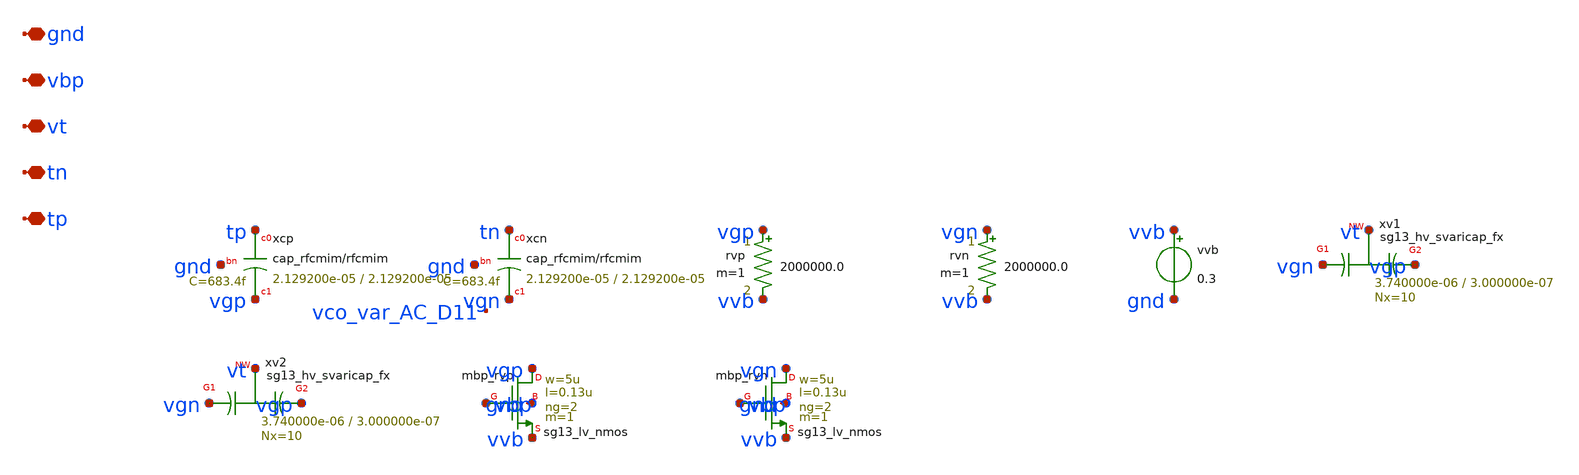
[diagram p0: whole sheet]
** sch_path: analog/vco/sch/vco_var.sch
**.subckt vco_var tp tn vt vbp gnd
*.iopin tp
*.iopin tn
*.iopin vt
*.iopin vbp
*.iopin gnd
Xxcp tp vgp gnd cap_rfcmim w=2.129200e-05 l=2.129200e-05 wfeed=5.0e-6 m=1 mm_ok=1
Xxcn tn vgn gnd cap_rfcmim w=2.129200e-05 l=2.129200e-05 wfeed=5.0e-6 m=1 mm_ok=1
rvp vgp vvb 2000000.0 m=1
rvn vgn vvb 2000000.0 m=1
vvb vvb gnd 0.3
Xxv1 vgn vt vgp sub! sg13_hv_svaricap_fx w=3.740000e-06 l=3.000000e-07 Nx=10 mm_ok=1
Xxv2 vgn vt vgp sub! sg13_hv_svaricap_fx w=3.740000e-06 l=3.000000e-07 Nx=10 mm_ok=1
Xmbp_rvp vgp vbp vvb gnd sg13_lv_nmos w=5u l=0.13u ng=2 m=1 mm_ok=1
Xmbp_rvn vgn vbp vvb gnd sg13_lv_nmos w=5u l=0.13u ng=2 m=1 mm_ok=1
**.ends
.end
